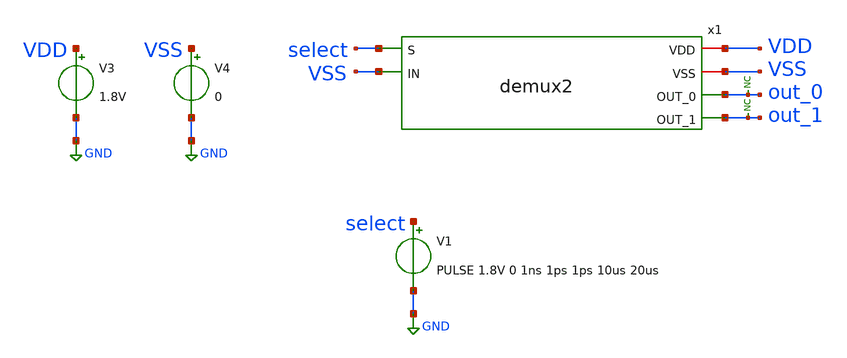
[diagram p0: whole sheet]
** sch_path: xschem/tests/demux2/demux2_switching_test.sch
**.subckt demux2_switching_test
V3 VDD GND 1.8V
V4 VSS GND 0
x1 select VDD VSS out_0 VSS out_1 demux2
V1 select GND PULSE 1.8V 0 1ns 1ps 1ps 10us 20us
* noconn out_0
* noconn out_1
**** begin user architecture code
 .lib $::SKYWATER_MODELS/sky130.lib.spice tt
.include $::SKYWATER_STDCELLS/sky130_fd_sc_hd.spice


.options acct list
.temp 25
*vvcc VDD 0 dc 1.8
*vvss VSS 0 0
.control
save all
tran 0.001n 4n
plot select out_0 out_1
write demux2_switching_test.raw
.endc


**** end user architecture code
**.ends

* expanding   symbol:  src/demux2/demux2.sym # of pins=6
** sym_path: xschem/src/demux2/demux2.sym
** sch_path: xschem/src/demux2/demux2.sch
.subckt demux2 S VDD VSS OUT_0 IN OUT_1
*.ipin S
*.opin OUT_0
*.ipin IN
*.opin OUT_1
*.iopin VDD
*.iopin VSS
x1 net1 IN VSS VSS VDD VDD OUT_0 sky130_fd_sc_hd__and2_0
x2 S IN VSS VSS VDD VDD OUT_1 sky130_fd_sc_hd__and2_0
x3 S VSS VSS VDD VDD net1 sky130_fd_sc_hd__inv_1
.ends

.GLOBAL GND
.end
